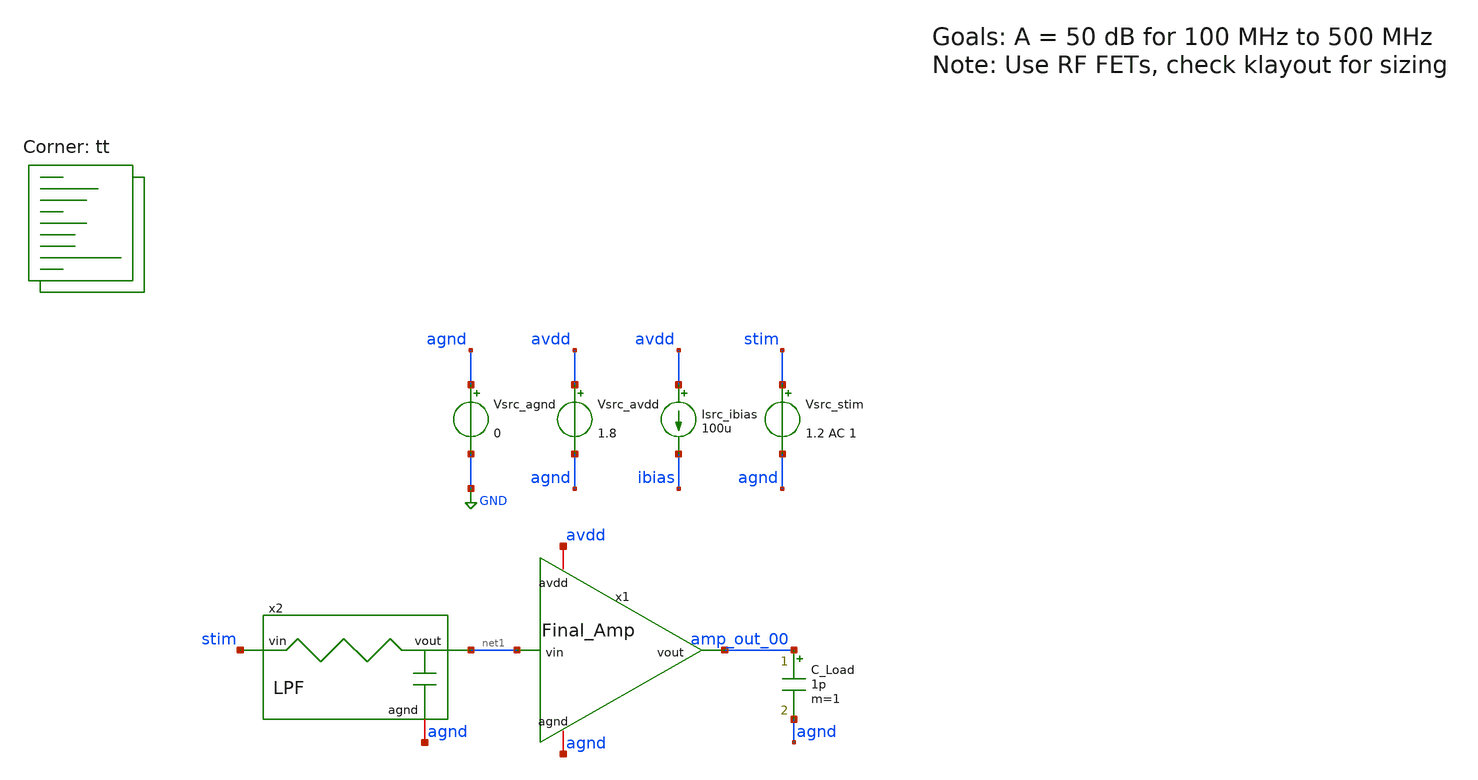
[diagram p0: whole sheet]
** sch_path: AMP/TB_Final_Amp.sch
**.subckt TB_Final_Amp
x1 amp_out_00 net1 agnd avdd Final_Amp
Vsrc_agnd agnd GND 0
Vsrc_avdd avdd agnd 1.8
Vsrc_stim stim agnd 1.2 AC 1
Isrc_ibias avdd ibias 100u
C_Load amp_out_00 agnd 1p m=1
x2 stim net1 agnd LPF
**** begin user architecture code

* this option enables mos model bin
* selection based on W/NF instead of W


.option savecurrents

.control
save all

save @m.x1.xm1.msky130_fd_pr__nfet_01v8[gm]
save @m.x1.xm2.msky130_fd_pr__nfet_01v8[gm]
save @m.x1.xm3.msky130_fd_pr__nfet_01v8[gm]
save @m.x1.xm4.msky130_fd_pr__nfet_01v8[gm]

op

* Print newline
echo

* Print stats for each MOSFET
* xm1 xm2 xm3 xm4
foreach mos xm1
 * Save stats
 let vth   = @m.x1.{$mos}.msky130_fd_pr__nfet_01v8[vth]
 let vdsat = @m.x1.{$mos}.msky130_fd_pr__nfet_01v8[vdsat]
 let gm    = @m.x1.{$mos}.msky130_fd_pr__nfet_01v8[gm]
 let gds   = @m.x1.{$mos}.msky130_fd_pr__nfet_01v8[gds]

 * Print stats
 echo Stats for $mos:
 print vth
 print vdsat
 print gm
 print gds

 * Print newline
 echo

end

* Print region of operation
echo Regions of Operation:
foreach nmos xm1
 * Save stats
 let vds = @m.x1.{$nmos}.msky130_fd_pr__nfet_01v8[vds]
 let vgs = @m.x1.{$nmos}.msky130_fd_pr__nfet_01v8[vgs]
 let vth = @m.x1.{$nmos}.msky130_fd_pr__nfet_01v8[vth]

 * Check and print regions
 if (vgs <= vth)
  echo $nmos: N Cutoff
 elseif (vds <= (vgs - vth))
  echo $nmos: N Triode
 else
  echo $nmos: N Saturation
 end
end

* Print newline
echo

* Sweep frequency
write TB_Final_Amp.raw
set appendwrite
ac dec 100 1 1e11
remzerovec

* Calculate gain
let ratio_00 = v(amp_out_00)/v(stim)

let gain_00 = db(mag(ratio_00))

write TB_Final_Amp.raw

.endc


.lib $::SKYWATER_MODELS/sky130.lib.spice tt
**** end user architecture code
**.ends
.GLOBAL GND
.end
